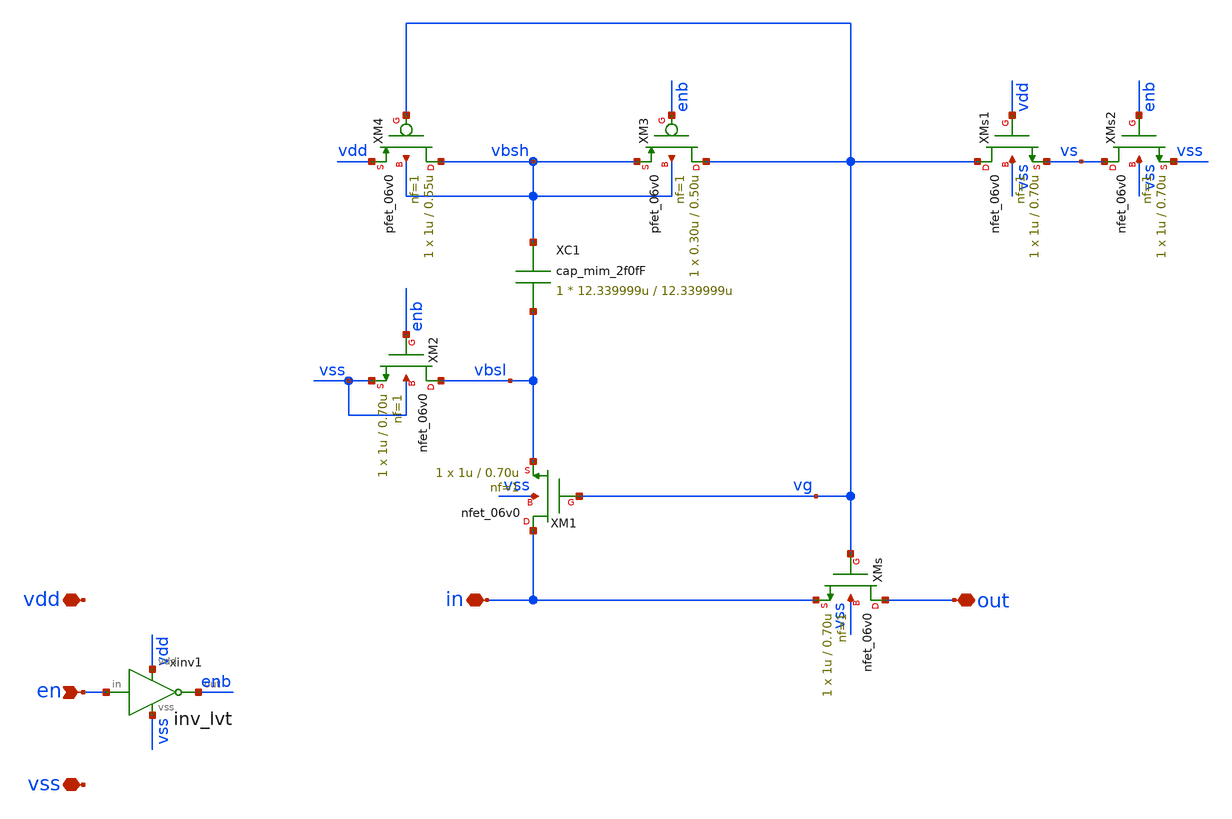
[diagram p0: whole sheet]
** sch_path: xschem/switches/bootstrapped_sw_hv.sch
**.subckt bootstrapped_sw_hv out en vss vdd in
*.iopin out
*.ipin en
*.iopin vss
*.iopin vdd
*.iopin in
xinv1 vdd en enb vss inv_lvt
XMs out vg in vss nfet_06v0 L=0.70u W=1u nf=1 ad='int((nf+1)/2) * W/nf * 0.18u' as='int((nf+2)/2) * W/nf * 0.18u'
+ pd='2*int((nf+1)/2) * (W/nf + 0.18u)' ps='2*int((nf+2)/2) * (W/nf + 0.18u)' nrd='0.18u / W' nrs='0.18u / W'
+ sa=0 sb=0 sd=0 m=1
XM4 vbsh vg vdd vbsh pfet_06v0 L=0.55u W=1u nf=1 ad='int((nf+1)/2) * W/nf * 0.18u' as='int((nf+2)/2) * W/nf * 0.18u'
+ pd='2*int((nf+1)/2) * (W/nf + 0.18u)' ps='2*int((nf+2)/2) * (W/nf + 0.18u)' nrd='0.18u / W' nrs='0.18u / W'
+ sa=0 sb=0 sd=0 m=1
XM3 vg enb vbsh vbsh pfet_06v0 L=0.50u W=0.30u nf=1 ad='int((nf+1)/2) * W/nf * 0.18u' as='int((nf+2)/2) * W/nf * 0.18u'
+ pd='2*int((nf+1)/2) * (W/nf + 0.18u)' ps='2*int((nf+2)/2) * (W/nf + 0.18u)' nrd='0.18u / W' nrs='0.18u / W'
+ sa=0 sb=0 sd=0 m=1
XMs2 vs enb vss vss nfet_06v0 L=0.70u W=1u nf=1 ad='int((nf+1)/2) * W/nf * 0.18u' as='int((nf+2)/2) * W/nf * 0.18u'
+ pd='2*int((nf+1)/2) * (W/nf + 0.18u)' ps='2*int((nf+2)/2) * (W/nf + 0.18u)' nrd='0.18u / W' nrs='0.18u / W'
+ sa=0 sb=0 sd=0 m=1
XMs1 vg vdd vs vss nfet_06v0 L=0.70u W=1u nf=1 ad='int((nf+1)/2) * W/nf * 0.18u' as='int((nf+2)/2) * W/nf * 0.18u'
+ pd='2*int((nf+1)/2) * (W/nf + 0.18u)' ps='2*int((nf+2)/2) * (W/nf + 0.18u)' nrd='0.18u / W' nrs='0.18u / W'
+ sa=0 sb=0 sd=0 m=1
XM1 in vg vbsl vss nfet_06v0 L=0.70u W=1u nf=1 ad='int((nf+1)/2) * W/nf * 0.18u' as='int((nf+2)/2) * W/nf * 0.18u'
+ pd='2*int((nf+1)/2) * (W/nf + 0.18u)' ps='2*int((nf+2)/2) * (W/nf + 0.18u)' nrd='0.18u / W' nrs='0.18u / W'
+ sa=0 sb=0 sd=0 m=1
XM2 vbsl enb vss vss nfet_06v0 L=0.70u W=1u nf=1 ad='int((nf+1)/2) * W/nf * 0.18u' as='int((nf+2)/2) * W/nf * 0.18u'
+ pd='2*int((nf+1)/2) * (W/nf + 0.18u)' ps='2*int((nf+2)/2) * (W/nf + 0.18u)' nrd='0.18u / W' nrs='0.18u / W'
+ sa=0 sb=0 sd=0 m=1
XC1 vbsh vbsl cap_mim_2f0fF c_width=12.339999u c_length=12.339999u m=1
**.ends

* expanding   symbol:  logic/inv_lvt.sym # of pins=4
** sym_path: logic/inv_lvt.sym
** sch_path: logic/inv_lvt.sch
.subckt inv_lvt vdd in out vss
*.iopin vdd
*.iopin vss
*.ipin in
*.opin out
XM1 out in vss vss nfet_06v0 L=0.70u W=1u nf=1 ad='int((nf+1)/2) * W/nf * 0.18u' as='int((nf+2)/2) * W/nf * 0.18u'
+ pd='2*int((nf+1)/2) * (W/nf + 0.18u)' ps='2*int((nf+2)/2) * (W/nf + 0.18u)' nrd='0.18u / W' nrs='0.18u / W'
+ sa=0 sb=0 sd=0 m=1
XM2 out in vdd vdd pfet_06v0 L=0.55u W=1u nf=1 ad='int((nf+1)/2) * W/nf * 0.18u' as='int((nf+2)/2) * W/nf * 0.18u'
+ pd='2*int((nf+1)/2) * (W/nf + 0.18u)' ps='2*int((nf+2)/2) * (W/nf + 0.18u)' nrd='0.18u / W' nrs='0.18u / W'
+ sa=0 sb=0 sd=0 m=1
.ends

.end
